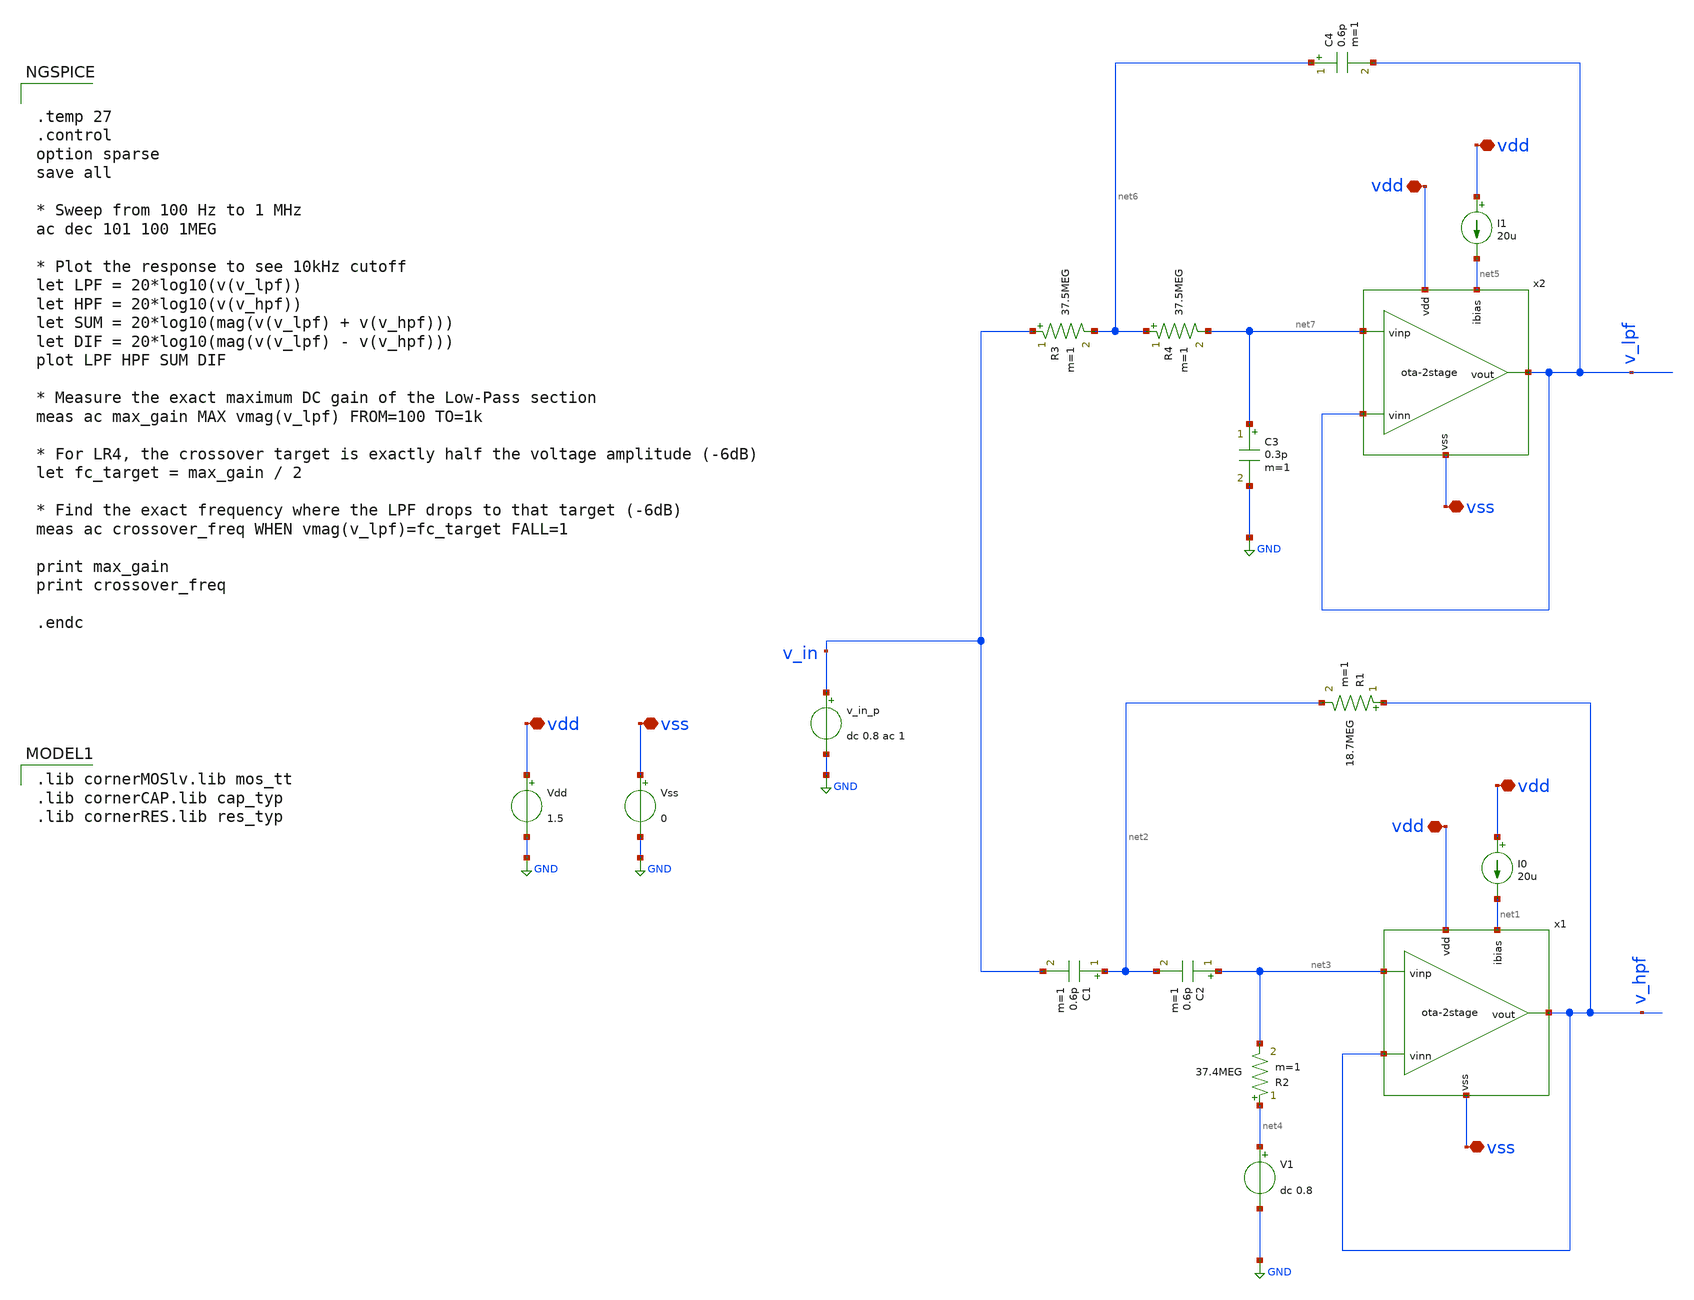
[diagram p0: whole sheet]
** sch_path: testbench/ota-2stage_tb-sk-LR2.sch
**.subckt ota-2stage_tb-sk-LR2 vdd vdd vdd vss vss vdd vdd vss
*.iopin vdd
*.iopin vdd
*.iopin vdd
*.iopin vss
*.iopin vss
*.iopin vdd
*.iopin vdd
*.iopin vss
I0 vdd net1 20u
Vdd vdd GND 1.5
Vss vss GND 0
v_in_p v_in GND dc 0.8 ac 1
x1 vdd net1 v_hpf v_hpf net3 vss ota-2stage
R1 v_hpf net2 18.7MEG m=1
R2 net4 net3 37.4MEG m=1
C1 net2 v_in 0.6p m=1
C2 net3 net2 0.6p m=1
V1 net4 GND dc 0.8
I1 vdd net5 20u
R3 v_in net6 37.5MEG m=1
R4 net6 net7 37.5MEG m=1
C3 net7 GND 0.3p m=1
C4 net6 v_lpf 0.6p m=1
x2 vdd net5 v_lpf v_lpf net7 vss ota-2stage
**** begin user architecture code
 .lib cornerMOSlv.lib mos_tt
.lib cornerCAP.lib cap_typ
.lib cornerRES.lib res_typ



.temp 27
.control
option sparse
save all

* Sweep from 100 Hz to 1 MHz
ac dec 101 100 1MEG

* Plot the response to see 10kHz cutoff
let LPF = 20*log10(v(v_lpf))
let HPF = 20*log10(v(v_hpf))
let SUM = 20*log10(mag(v(v_lpf) + v(v_hpf)))
let DIF = 20*log10(mag(v(v_lpf) - v(v_hpf)))
plot LPF HPF SUM DIF

* Measure the exact maximum DC gain of the Low-Pass section
meas ac max_gain MAX vmag(v_lpf) FROM=100 TO=1k

* For LR4, the crossover target is exactly half the voltage amplitude (-6dB)
let fc_target = max_gain / 2

* Find the exact frequency where the LPF drops to that target (-6dB)
meas ac crossover_freq WHEN vmag(v_lpf)=fc_target FALL=1

print max_gain
print crossover_freq

.endc


**** end user architecture code
**.ends
.GLOBAL GND
.end
